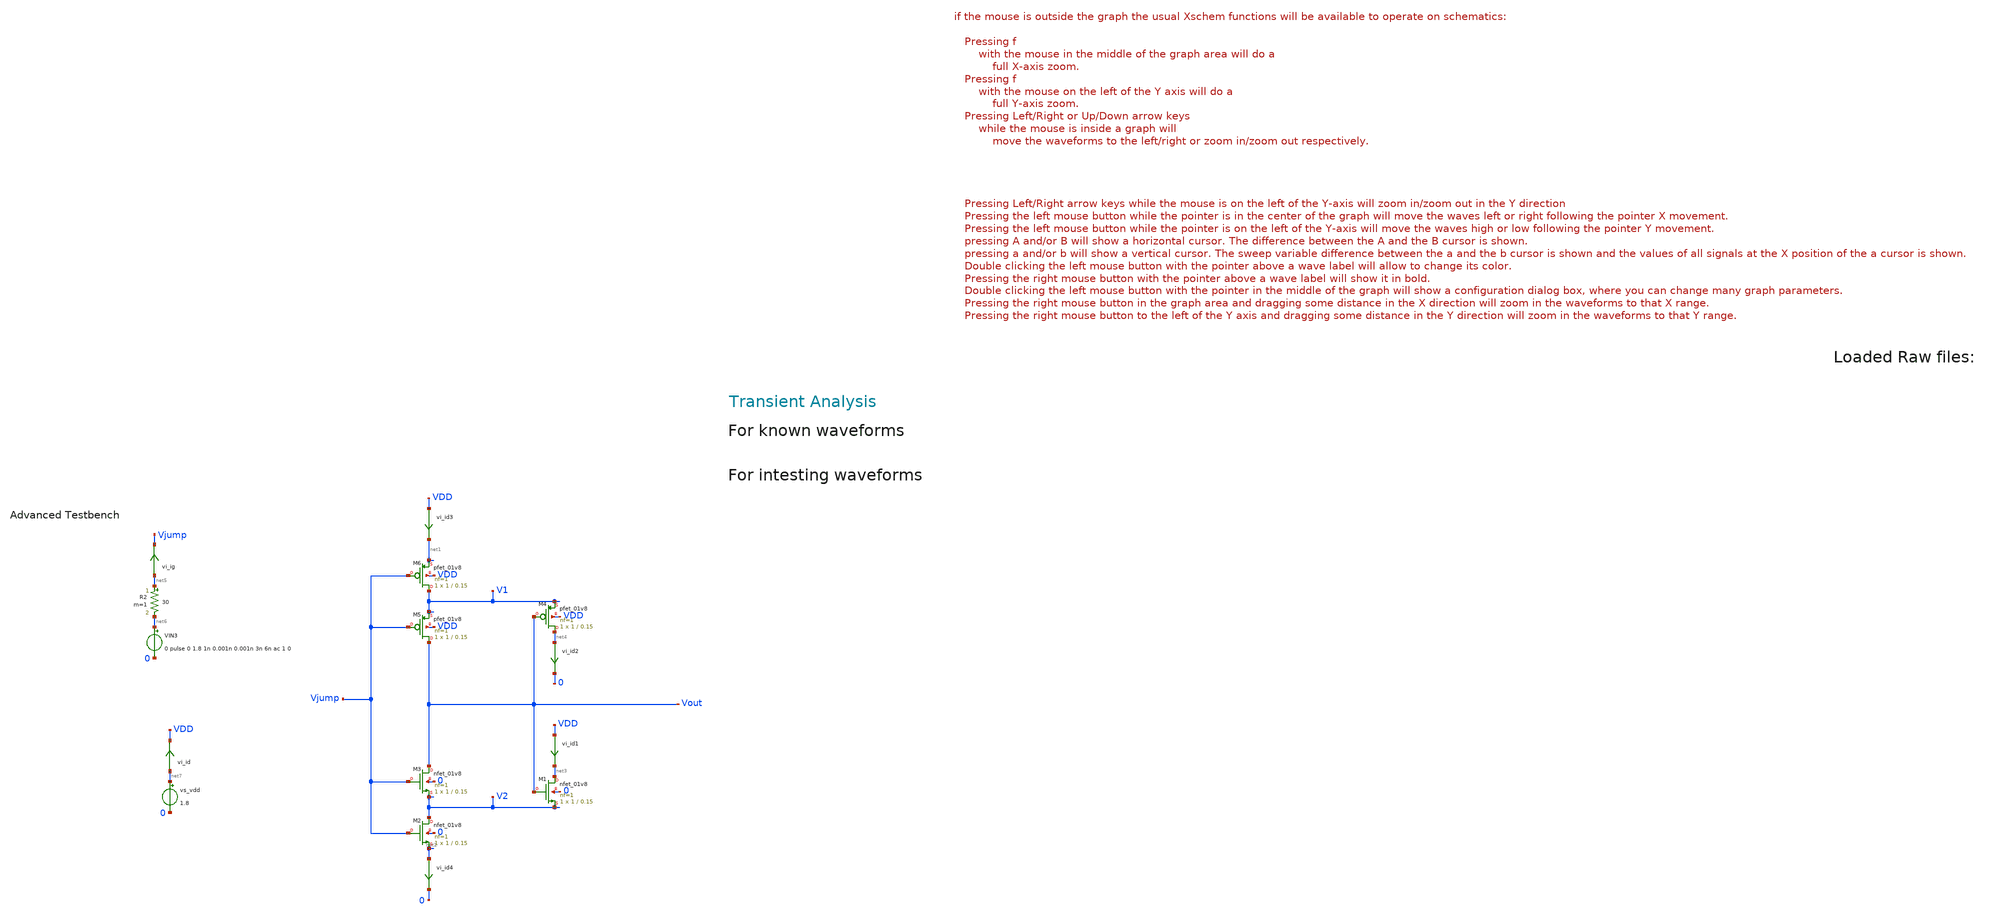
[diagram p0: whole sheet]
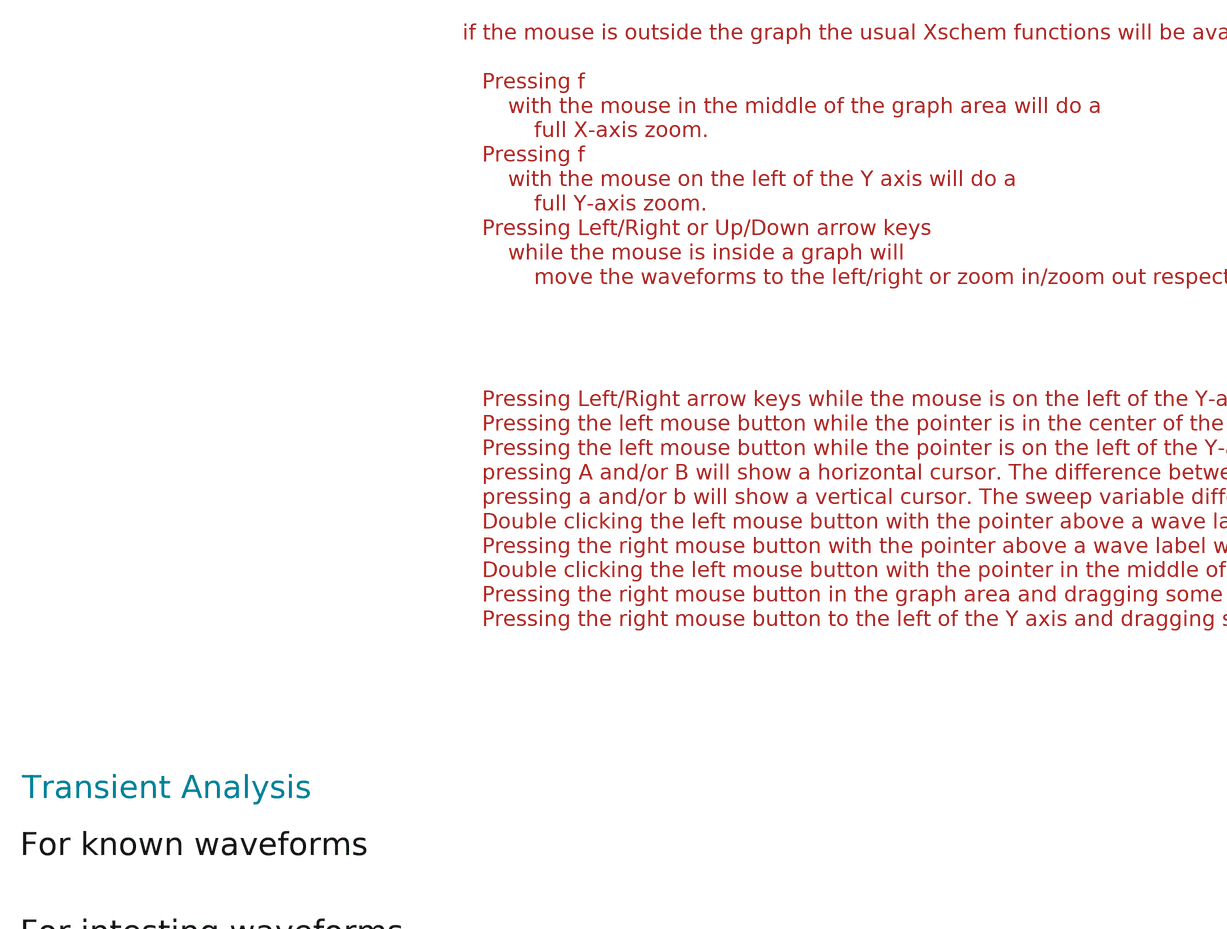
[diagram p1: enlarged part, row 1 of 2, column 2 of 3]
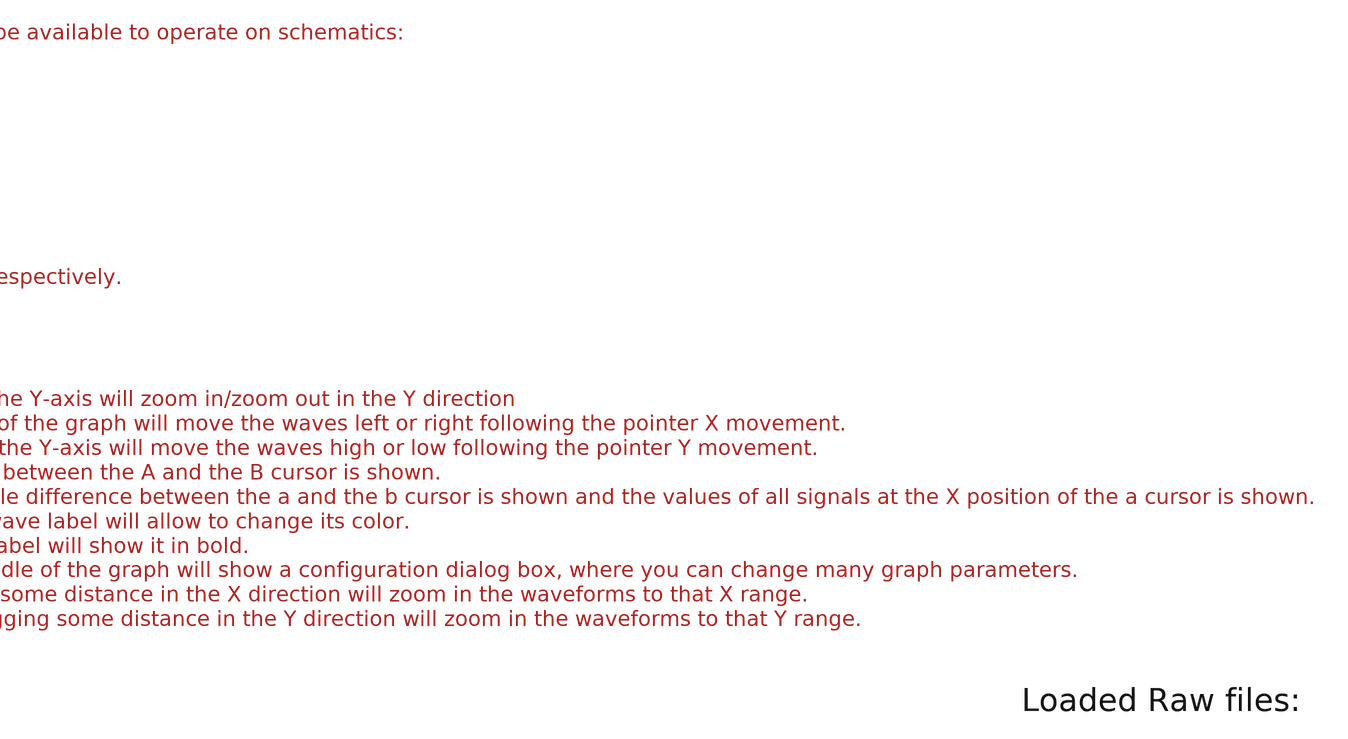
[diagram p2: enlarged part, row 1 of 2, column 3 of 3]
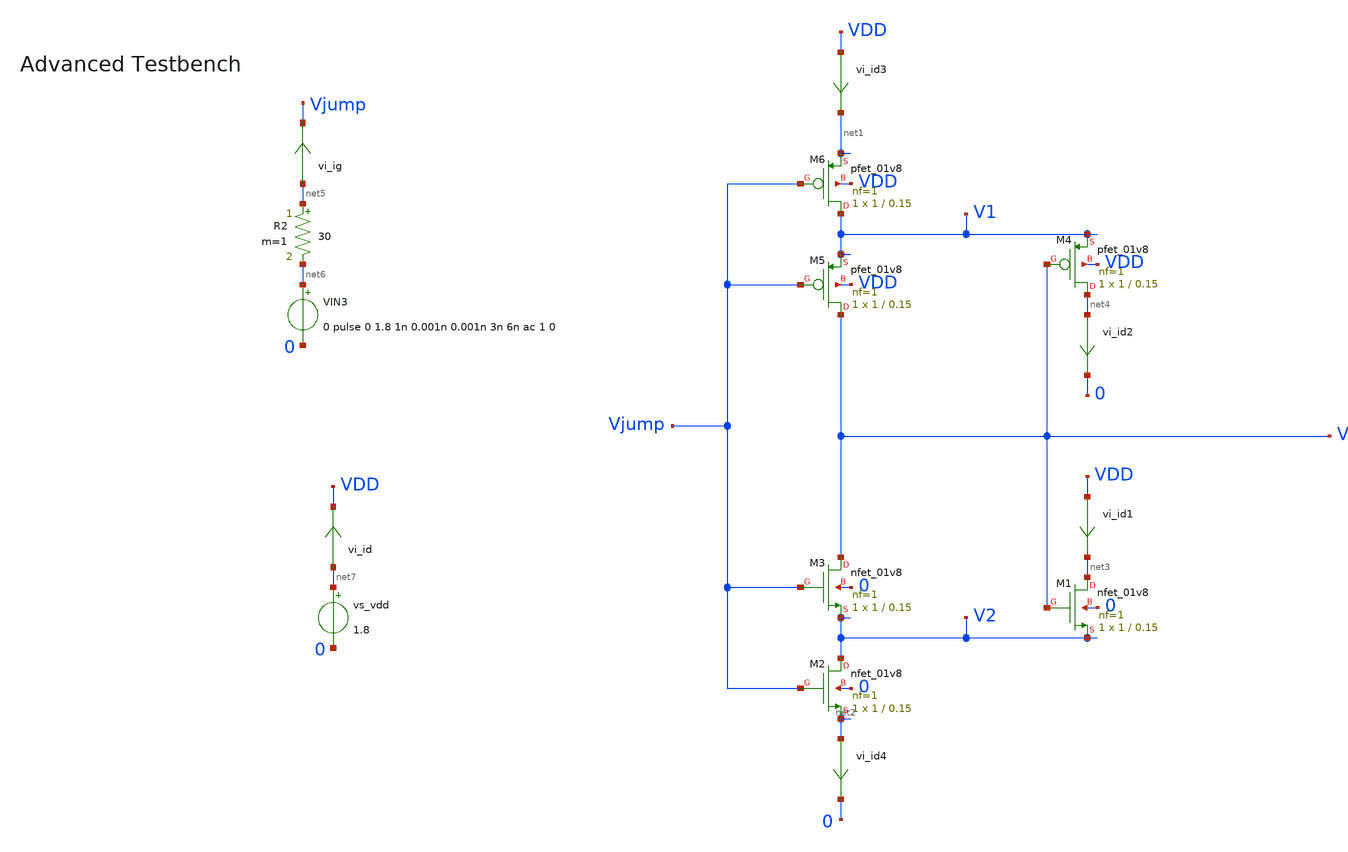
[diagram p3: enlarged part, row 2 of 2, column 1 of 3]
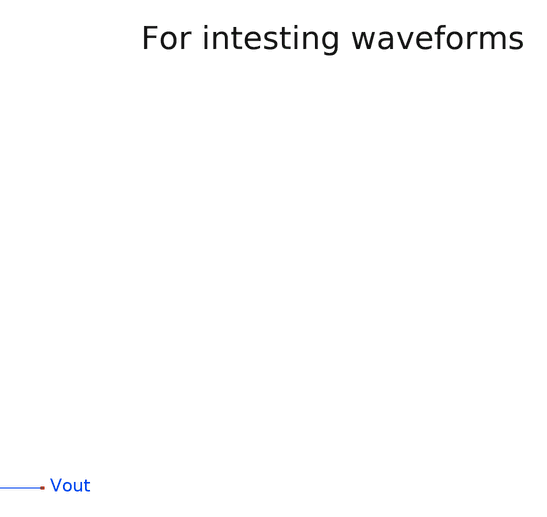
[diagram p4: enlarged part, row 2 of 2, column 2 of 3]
** sch_path: tt10-hdl/tt_um_test_commit/xschem/T1/schmTrigg/schmTrigg_slewrate_tb.sch
* Copyright (C) 1998-2024 Stefan Frederik Schippers
* This program is free software; you can redistribute it and/or modify
* it under the terms of the GNU General Public License as published by
* the Free Software Foundation; either version 2 of the License, or
* (at your option) any later version.
* This program is distributed in the hope that it will be useful,
* but WITHOUT ANY WARRANTY; without even the implied warranty of
* MERCHANTABILITY or FITNESS FOR A PARTICULAR PURPOSE.  See the
* GNU General Public License for more details.
* You should have received a copy of the GNU General Public License
* along with this program; if not, write to the Free Software
**.subckt schmTrigg_slewrate_tb
vs_vdd net7 0 1.8
XM1 net3 Vout V2 0 sky130_fd_pr__nfet_01v8 L=0.15 W=1 nf=1 ad='int((1 + 1)/2) * 1 / 1 * 0.29' as='int((1 + 2)/2) * 1 / 1 * 0.29'
+ pd='2*int((1 + 1)/2) * (1 / 1 + 0.29)' ps='2*int((1 + 2)/2) * (1 / 1 + 0.29)' nrd='0.29 / 1 ' nrs='0.29 / 1 '
+ sa=0 sb=0 sd=0 mult=1 m=1
XM2 V2 Vjump net2 0 sky130_fd_pr__nfet_01v8 L=0.15 W=1 nf=1 ad='int((1 + 1)/2) * 1 / 1 * 0.29' as='int((1 + 2)/2) * 1 / 1 * 0.29'
+ pd='2*int((1 + 1)/2) * (1 / 1 + 0.29)' ps='2*int((1 + 2)/2) * (1 / 1 + 0.29)' nrd='0.29 / 1 ' nrs='0.29 / 1 '
+ sa=0 sb=0 sd=0 mult=1 m=1
XM3 Vout Vjump V2 0 sky130_fd_pr__nfet_01v8 L=0.15 W=1 nf=1 ad='int((1 + 1)/2) * 1 / 1 * 0.29' as='int((1 + 2)/2) * 1 / 1 * 0.29'
+ pd='2*int((1 + 1)/2) * (1 / 1 + 0.29)' ps='2*int((1 + 2)/2) * (1 / 1 + 0.29)' nrd='0.29 / 1 ' nrs='0.29 / 1 '
+ sa=0 sb=0 sd=0 mult=1 m=1
XM4 net4 Vout V1 VDD sky130_fd_pr__pfet_01v8 L=0.15 W=1 nf=1 ad='int((nf+1)/2) * W/nf * 0.29' as='int((nf+2)/2) * W/nf * 0.29'
+ pd='2*int((nf+1)/2) * (W/nf + 0.29)' ps='2*int((nf+2)/2) * (W/nf + 0.29)' nrd='0.29 / W' nrs='0.29 / W'
+ sa=0 sb=0 sd=0 mult=1 m=1
XM5 Vout Vjump V1 VDD sky130_fd_pr__pfet_01v8 L=0.15 W=1 nf=1 ad='int((nf+1)/2) * W/nf * 0.29' as='int((nf+2)/2) * W/nf * 0.29'
+ pd='2*int((nf+1)/2) * (W/nf + 0.29)' ps='2*int((nf+2)/2) * (W/nf + 0.29)' nrd='0.29 / W' nrs='0.29 / W'
+ sa=0 sb=0 sd=0 mult=1 m=1
XM6 V1 Vjump net1 VDD sky130_fd_pr__pfet_01v8 L=0.15 W=1 nf=1 ad='int((nf+1)/2) * W/nf * 0.29' as='int((nf+2)/2) * W/nf * 0.29'
+ pd='2*int((nf+1)/2) * (W/nf + 0.29)' ps='2*int((nf+2)/2) * (W/nf + 0.29)' nrd='0.29 / W' nrs='0.29 / W'
+ sa=0 sb=0 sd=0 mult=1 m=1
VIN3 net6 0 0 pulse 0 1.8 1n 0.001n 0.001n 3n 6n ac 1 0
vi_ig net5 Vjump 0
.save i(vi_ig)
R2 net5 net6 30 m=1
vi_id net7 VDD 0
.save i(vi_id)
vi_id1 VDD net3 0
.save i(vi_id1)
vi_id2 net4 0 0
.save i(vi_id2)
vi_id3 VDD net1 0
.save i(vi_id3)
vi_id4 net2 0 0
.save i(vi_id4)
**** begin user architecture code



.temp 30

.option savecurrents
.save all *@m1[gm]
.control
  save all alli
  op
  remzerovec
  write schmTriggTran.raw
  set appendwrite

  tran 0.001n 10n
  remzerovec
  write schmTriggTran.raw




  *quit 0




.endc





** opencircuitdesign pdks install
.lib $::SKYWATER_MODELS/sky130.lib.spice tt
.include $::SKYWATER_STDCELLS/sky130_fd_sc_hd.spice


**** end user architecture code
**.ends
.end
